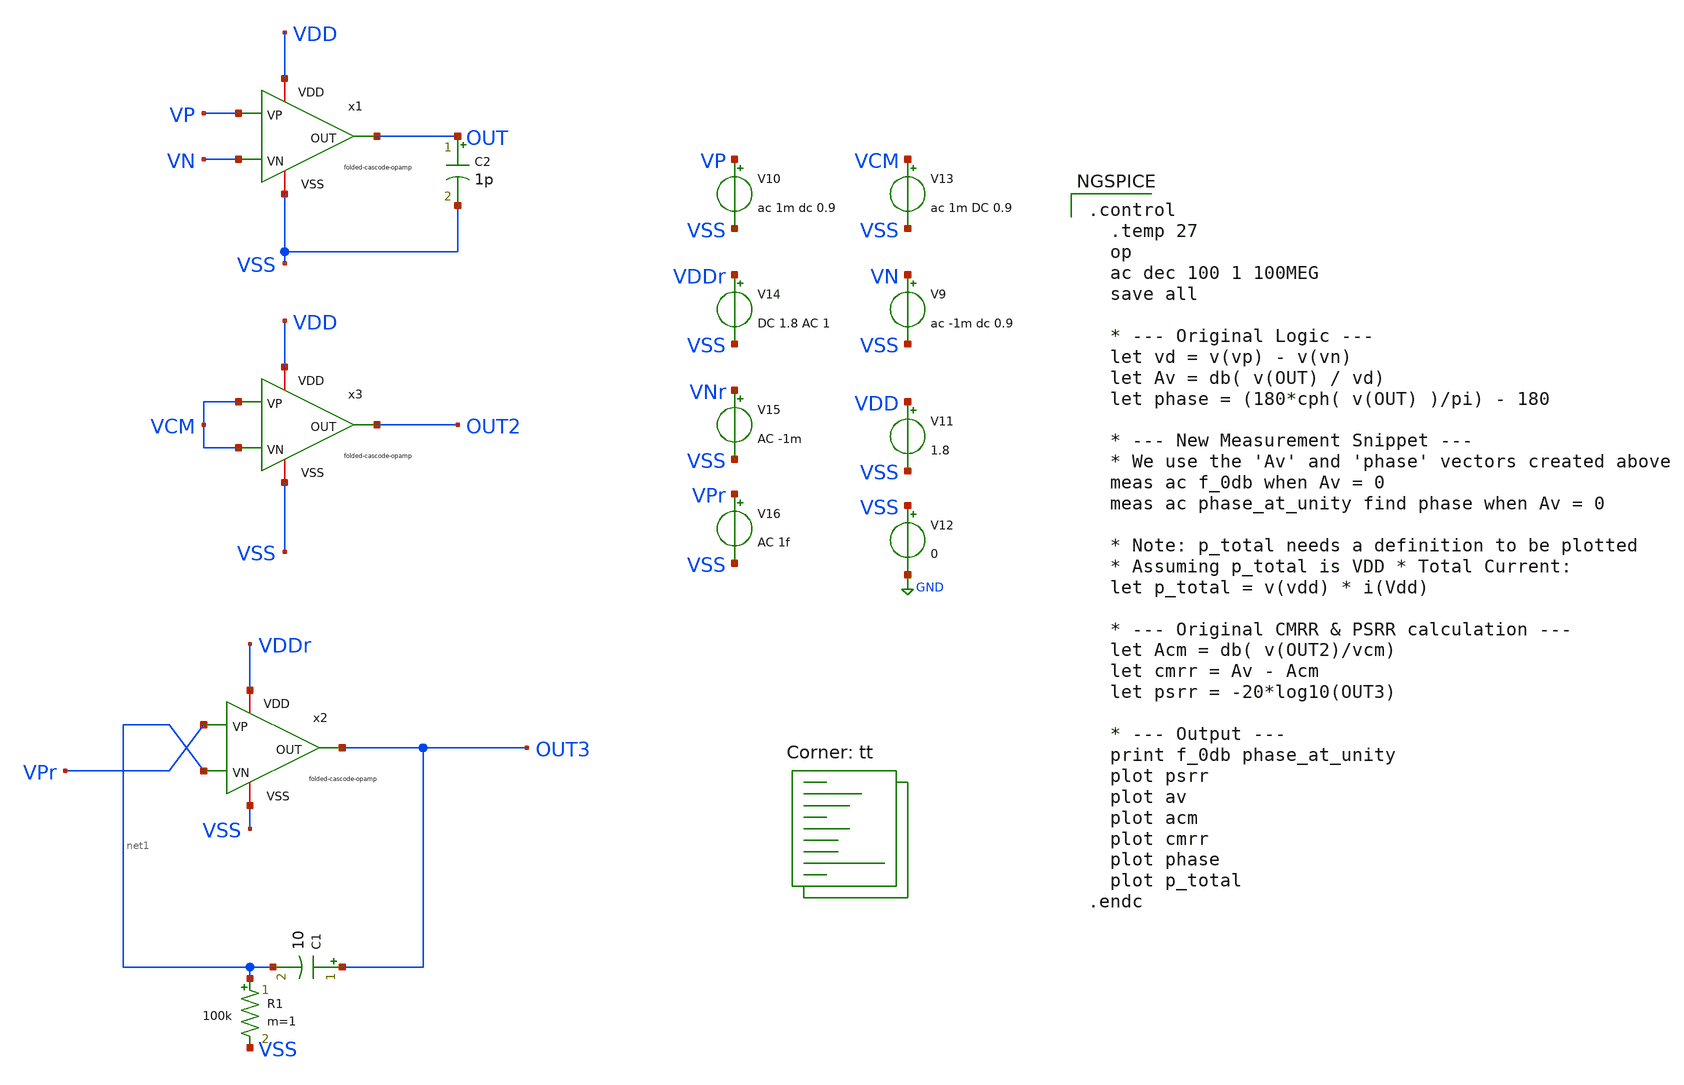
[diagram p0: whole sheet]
** sch_path: bandgap/bgr-opamp2/tb_ac.sch
**.subckt tb_ac
C2 OUT VSS 1p m=1
V9 VN VSS ac -1m dc 0.9
V10 VP VSS ac 1m dc 0.9
V11 VDD VSS 1.8
V12 VSS GND 0
V13 VCM VSS ac 1m DC 0.9
V14 VDDr VSS DC 1.8 AC 1
V15 VNr VSS AC -1m
V16 VPr VSS AC 1f
x1 OUT VDD VP VN VSS folded-cascode-opamp
x2 OUT3 VDDr VPr net1 VSS folded-cascode-opamp
x3 OUT2 VDD VCM VCM VSS folded-cascode-opamp
C1 OUT3 net1 10 m=1
R1 net1 VSS 100k m=1
**** begin user architecture code

.control
  .temp 27
  op
  ac dec 100 1 100MEG
  save all

  * --- Original Logic ---
  let vd = v(vp) - v(vn)
  let Av = db( v(OUT) / vd)
  let phase = (180*cph( v(OUT) )/pi) - 180

  * --- New Measurement Snippet ---
  * We use the 'Av' and 'phase' vectors created above
  meas ac f_0db when Av = 0
  meas ac phase_at_unity find phase when Av = 0

  * Note: p_total needs a definition to be plotted
  * Assuming p_total is VDD * Total Current:
  let p_total = v(vdd) * i(Vdd)

  * --- Original CMRR & PSRR calculation ---
  let Acm = db( v(OUT2)/vcm)
  let cmrr = Av - Acm
  let psrr = -20*log10(OUT3)

  * --- Output ---
  print f_0db phase_at_unity
  plot psrr
  plot av
  plot acm
  plot cmrr
  plot phase
  plot p_total
.endc



.lib $::SKYWATER_MODELS/sky130.lib.spice tt
**** end user architecture code
**.ends

* expanding   symbol:  afe-icdec-teknofest-2026/bandgap/bgr-opamp2/folded-cascode-opamp.sym # of
*+ pins=5
** sym_path: bandgap/bgr-opamp2/folded-cascode-opamp.sym
** sch_path: bandgap/bgr-opamp2/folded-cascode-opamp.sch
.subckt folded-cascode-opamp OUT VDD VP VN VSS
*.iopin VSS
*.iopin VDD
*.ipin VP
*.ipin VN
*.opin OUT
XR10 VSS net5 VSS sky130_fd_pr__res_high_po_1p41 L=0.235 mult=1 m=1
XM19 net2 net2 VSS GND sky130_fd_pr__nfet_01v8_lvt L=0.5 W=6.4 nf=1 ad='int((nf+1)/2) * W/nf * 0.29'
+ as='int((nf+2)/2) * W/nf * 0.29' pd='2*int((nf+1)/2) * (W/nf + 0.29)' ps='2*int((nf+2)/2) * (W/nf + 0.29)'
+ nrd='0.29 / W' nrs='0.29 / W' sa=0 sb=0 sd=0 mult=1 m=1
XM20 net3 net2 net5 GND sky130_fd_pr__nfet_01v8_lvt L=0.5 W=6.4 nf=1 ad='int((nf+1)/2) * W/nf * 0.29'
+ as='int((nf+2)/2) * W/nf * 0.29' pd='2*int((nf+1)/2) * (W/nf + 0.29)' ps='2*int((nf+2)/2) * (W/nf + 0.29)'
+ nrd='0.29 / W' nrs='0.29 / W' sa=0 sb=0 sd=0 mult=1 m=1
XM16 net4 net1 VDD VDD sky130_fd_pr__pfet_01v8_lvt L=0.5 W=20.8 nf=1 ad='int((nf+1)/2) * W/nf * 0.29'
+ as='int((nf+2)/2) * W/nf * 0.29' pd='2*int((nf+1)/2) * (W/nf + 0.29)' ps='2*int((nf+2)/2) * (W/nf + 0.29)'
+ nrd='0.29 / W' nrs='0.29 / W' sa=0 sb=0 sd=0 mult=1 m=1
XM13 net1 net1 VDD VDD sky130_fd_pr__pfet_01v8_lvt L=0.5 W=20.8 nf=1 ad='int((nf+1)/2) * W/nf * 0.29'
+ as='int((nf+2)/2) * W/nf * 0.29' pd='2*int((nf+1)/2) * (W/nf + 0.29)' ps='2*int((nf+2)/2) * (W/nf + 0.29)'
+ nrd='0.29 / W' nrs='0.29 / W' sa=0 sb=0 sd=0 mult=1 m=1
XM14 net2 net3 net4 VDD sky130_fd_pr__pfet_01v8_lvt L=0.5 W=20.8 nf=1 ad='int((nf+1)/2) * W/nf * 0.29'
+ as='int((nf+2)/2) * W/nf * 0.29' pd='2*int((nf+1)/2) * (W/nf + 0.29)' ps='2*int((nf+2)/2) * (W/nf + 0.29)'
+ nrd='0.29 / W' nrs='0.29 / W' sa=0 sb=0 sd=0 mult=1 m=1
XM17 net3 net3 net1 VDD sky130_fd_pr__pfet_01v8_lvt L=0.5 W=20.8 nf=1 ad='int((nf+1)/2) * W/nf * 0.29'
+ as='int((nf+2)/2) * W/nf * 0.29' pd='2*int((nf+1)/2) * (W/nf + 0.29)' ps='2*int((nf+2)/2) * (W/nf + 0.29)'
+ nrd='0.29 / W' nrs='0.29 / W' sa=0 sb=0 sd=0 mult=1 m=1
XM18 net6 net1 VDD VDD sky130_fd_pr__pfet_01v8_lvt L=0.5 W=20.8 nf=1 ad='int((nf+1)/2) * W/nf * 0.29'
+ as='int((nf+2)/2) * W/nf * 0.29' pd='2*int((nf+1)/2) * (W/nf + 0.29)' ps='2*int((nf+2)/2) * (W/nf + 0.29)'
+ nrd='0.29 / W' nrs='0.29 / W' sa=0 sb=0 sd=0 mult=1 m=1
XM21 net7 net3 net6 VDD sky130_fd_pr__pfet_01v8_lvt L=0.5 W=20.8 nf=1 ad='int((nf+1)/2) * W/nf * 0.29'
+ as='int((nf+2)/2) * W/nf * 0.29' pd='2*int((nf+1)/2) * (W/nf + 0.29)' ps='2*int((nf+2)/2) * (W/nf + 0.29)'
+ nrd='0.29 / W' nrs='0.29 / W' sa=0 sb=0 sd=0 mult=1 m=1
XM22 net7 net7 net9 GND sky130_fd_pr__nfet_01v8_lvt L=0.5 W=1.45 nf=1 ad='int((nf+1)/2) * W/nf * 0.29'
+ as='int((nf+2)/2) * W/nf * 0.29' pd='2*int((nf+1)/2) * (W/nf + 0.29)' ps='2*int((nf+2)/2) * (W/nf + 0.29)'
+ nrd='0.29 / W' nrs='0.29 / W' sa=0 sb=0 sd=0 mult=1 m=1
XM23 net9 net7 net8 GND sky130_fd_pr__nfet_01v8_lvt L=0.5 W=1.45 nf=1 ad='int((nf+1)/2) * W/nf * 0.29'
+ as='int((nf+2)/2) * W/nf * 0.29' pd='2*int((nf+1)/2) * (W/nf + 0.29)' ps='2*int((nf+2)/2) * (W/nf + 0.29)'
+ nrd='0.29 / W' nrs='0.29 / W' sa=0 sb=0 sd=0 mult=1 m=1
XM24 net8 net7 VSS GND sky130_fd_pr__nfet_01v8_lvt L=0.5 W=1.45 nf=1 ad='int((nf+1)/2) * W/nf * 0.29'
+ as='int((nf+2)/2) * W/nf * 0.29' pd='2*int((nf+1)/2) * (W/nf + 0.29)' ps='2*int((nf+2)/2) * (W/nf + 0.29)'
+ nrd='0.29 / W' nrs='0.29 / W' sa=0 sb=0 sd=0 mult=1 m=1
XM26 net16 VN net10 VDD sky130_fd_pr__pfet_01v8_lvt L=1.25 W=84 nf=1 ad='int((nf+1)/2) * W/nf * 0.29'
+ as='int((nf+2)/2) * W/nf * 0.29' pd='2*int((nf+1)/2) * (W/nf + 0.29)' ps='2*int((nf+2)/2) * (W/nf + 0.29)'
+ nrd='0.29 / W' nrs='0.29 / W' sa=0 sb=0 sd=0 mult=1 m=1
XM27 net15 VP net10 VDD sky130_fd_pr__pfet_01v8_lvt L=1.25 W=84 nf=1 ad='int((nf+1)/2) * W/nf * 0.29'
+ as='int((nf+2)/2) * W/nf * 0.29' pd='2*int((nf+1)/2) * (W/nf + 0.29)' ps='2*int((nf+2)/2) * (W/nf + 0.29)'
+ nrd='0.29 / W' nrs='0.29 / W' sa=0 sb=0 sd=0 mult=1 m=1
XM15 net10 OUT VDD VDD sky130_fd_pr__pfet_01v8_lvt L=1.25 W=20.8 nf=1 ad='int((nf+1)/2) * W/nf * 0.29'
+ as='int((nf+2)/2) * W/nf * 0.29' pd='2*int((nf+1)/2) * (W/nf + 0.29)' ps='2*int((nf+2)/2) * (W/nf + 0.29)'
+ nrd='0.29 / W' nrs='0.29 / W' sa=0 sb=0 sd=0 mult=1 m=1
XM25 net12 net1 VDD VDD sky130_fd_pr__pfet_01v8_lvt L=1.25 W=10.4 nf=1 ad='int((nf+1)/2) * W/nf * 0.29'
+ as='int((nf+2)/2) * W/nf * 0.29' pd='2*int((nf+1)/2) * (W/nf + 0.29)' ps='2*int((nf+2)/2) * (W/nf + 0.29)'
+ nrd='0.29 / W' nrs='0.29 / W' sa=0 sb=0 sd=0 mult=1 m=1
XM28 net13 net1 VDD VDD sky130_fd_pr__pfet_01v8_lvt L=1.25 W=10.4 nf=1 ad='int((nf+1)/2) * W/nf * 0.29'
+ as='int((nf+2)/2) * W/nf * 0.29' pd='2*int((nf+1)/2) * (W/nf + 0.29)' ps='2*int((nf+2)/2) * (W/nf + 0.29)'
+ nrd='0.29 / W' nrs='0.29 / W' sa=0 sb=0 sd=0 mult=1 m=1
XM29 net14 net3 net12 VDD sky130_fd_pr__pfet_01v8_lvt L=1.25 W=10.4 nf=1 ad='int((nf+1)/2) * W/nf * 0.29'
+ as='int((nf+2)/2) * W/nf * 0.29' pd='2*int((nf+1)/2) * (W/nf + 0.29)' ps='2*int((nf+2)/2) * (W/nf + 0.29)'
+ nrd='0.29 / W' nrs='0.29 / W' sa=0 sb=0 sd=0 mult=1 m=1
XM30 net11 net3 net13 VDD sky130_fd_pr__pfet_01v8_lvt L=1.25 W=10.4 nf=1 ad='int((nf+1)/2) * W/nf * 0.29'
+ as='int((nf+2)/2) * W/nf * 0.29' pd='2*int((nf+1)/2) * (W/nf + 0.29)' ps='2*int((nf+2)/2) * (W/nf + 0.29)'
+ nrd='0.29 / W' nrs='0.29 / W' sa=0 sb=0 sd=0 mult=1 m=1
XM31 net14 net7 net16 GND sky130_fd_pr__nfet_01v8_lvt L=1.25 W=2.4 nf=1 ad='int((nf+1)/2) * W/nf * 0.29'
+ as='int((nf+2)/2) * W/nf * 0.29' pd='2*int((nf+1)/2) * (W/nf + 0.29)' ps='2*int((nf+2)/2) * (W/nf + 0.29)'
+ nrd='0.29 / W' nrs='0.29 / W' sa=0 sb=0 sd=0 mult=1 m=1
XM32 net11 net7 net15 GND sky130_fd_pr__nfet_01v8_lvt L=1.25 W=2.4 nf=1 ad='int((nf+1)/2) * W/nf * 0.29'
+ as='int((nf+2)/2) * W/nf * 0.29' pd='2*int((nf+1)/2) * (W/nf + 0.29)' ps='2*int((nf+2)/2) * (W/nf + 0.29)'
+ nrd='0.29 / W' nrs='0.29 / W' sa=0 sb=0 sd=0 mult=1 m=1
XM33 net16 net11 VSS GND sky130_fd_pr__nfet_01v8_lvt L=1.25 W=2.4 nf=1 ad='int((nf+1)/2) * W/nf * 0.29'
+ as='int((nf+2)/2) * W/nf * 0.29' pd='2*int((nf+1)/2) * (W/nf + 0.29)' ps='2*int((nf+2)/2) * (W/nf + 0.29)'
+ nrd='0.29 / W' nrs='0.29 / W' sa=0 sb=0 sd=0 mult=1 m=1
XM34 net15 net11 VSS GND sky130_fd_pr__nfet_01v8_lvt L=1.25 W=2.4 nf=1 ad='int((nf+1)/2) * W/nf * 0.29'
+ as='int((nf+2)/2) * W/nf * 0.29' pd='2*int((nf+1)/2) * (W/nf + 0.29)' ps='2*int((nf+2)/2) * (W/nf + 0.29)'
+ nrd='0.29 / W' nrs='0.29 / W' sa=0 sb=0 sd=0 mult=1 m=1
XM35 OUT OUT VDD VDD sky130_fd_pr__pfet_01v8_lvt L=1.25 W=20.8 nf=1 ad='int((nf+1)/2) * W/nf * 0.29'
+ as='int((nf+2)/2) * W/nf * 0.29' pd='2*int((nf+1)/2) * (W/nf + 0.29)' ps='2*int((nf+2)/2) * (W/nf + 0.29)'
+ nrd='0.29 / W' nrs='0.29 / W' sa=0 sb=0 sd=0 mult=1 m=1
XM1 OUT net14 VSS GND sky130_fd_pr__nfet_01v8_lvt L=1.25 W=2.5 nf=1 ad='int((nf+1)/2) * W/nf * 0.29'
+ as='int((nf+2)/2) * W/nf * 0.29' pd='2*int((nf+1)/2) * (W/nf + 0.29)' ps='2*int((nf+2)/2) * (W/nf + 0.29)'
+ nrd='0.29 / W' nrs='0.29 / W' sa=0 sb=0 sd=0 mult=1 m=1
XC1 OUT net14 sky130_fd_pr__cap_mim_m3_1 W=25 L=25 MF=2 m=2
.ends

.GLOBAL GND
.end
